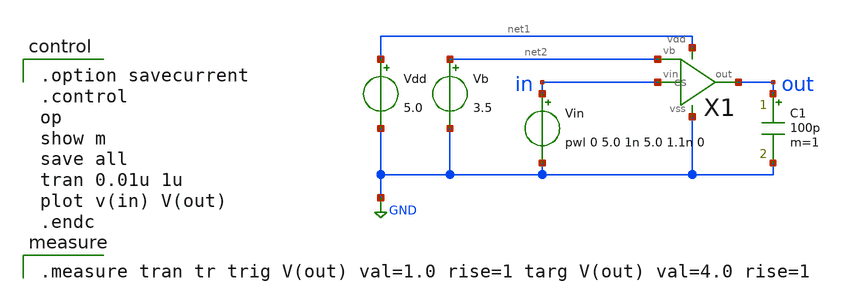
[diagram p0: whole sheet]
** sch_path: schematic/20250924_OSS_Workshop/ishikai/opamp/sample/cs_tran.sch
**.subckt cs_tran
Vdd net1 GND 5.0
Vb net2 GND 3.5
X1 in net2 out net1 GND cs
C1 out GND 100p m=1
Vin in GND pwl 0 5.0 1n 5.0 1.1n 0
**** begin user architecture code

.option savecurrent
.control
op
show m
save all
tran 0.01u 1u
plot v(in) V(out)
.endc


.measure tran tr trig V(out) val=1.0 rise=1 targ V(out) val=4.0 rise=1

 .include $::LIB/../ip62_models
**** end user architecture code
**.ends

* expanding   symbol:  cs.sym # of pins=5
** sym_path: schematic/20250924_OSS_Workshop/ishikai/opamp/sample/cs.sym
** sch_path: schematic/20250924_OSS_Workshop/ishikai/opamp/sample/cs.sch
.subckt cs vin vb out vdd vss
*.ipin vb
*.ipin vin
*.opin out
*.iopin vss
*.iopin vdd
XM6 out vb vdd vdd PMOS w=270u l=1u as=0 ad=0 ps=0 pd=0 nrd=0 nrs=0 m=1
XM7 out vin vss vss NMOS w=90u l=1u as=0 ad=0 ps=0 pd=0 nrd=0 nrs=0 m=1
.ends

.GLOBAL GND
.end
